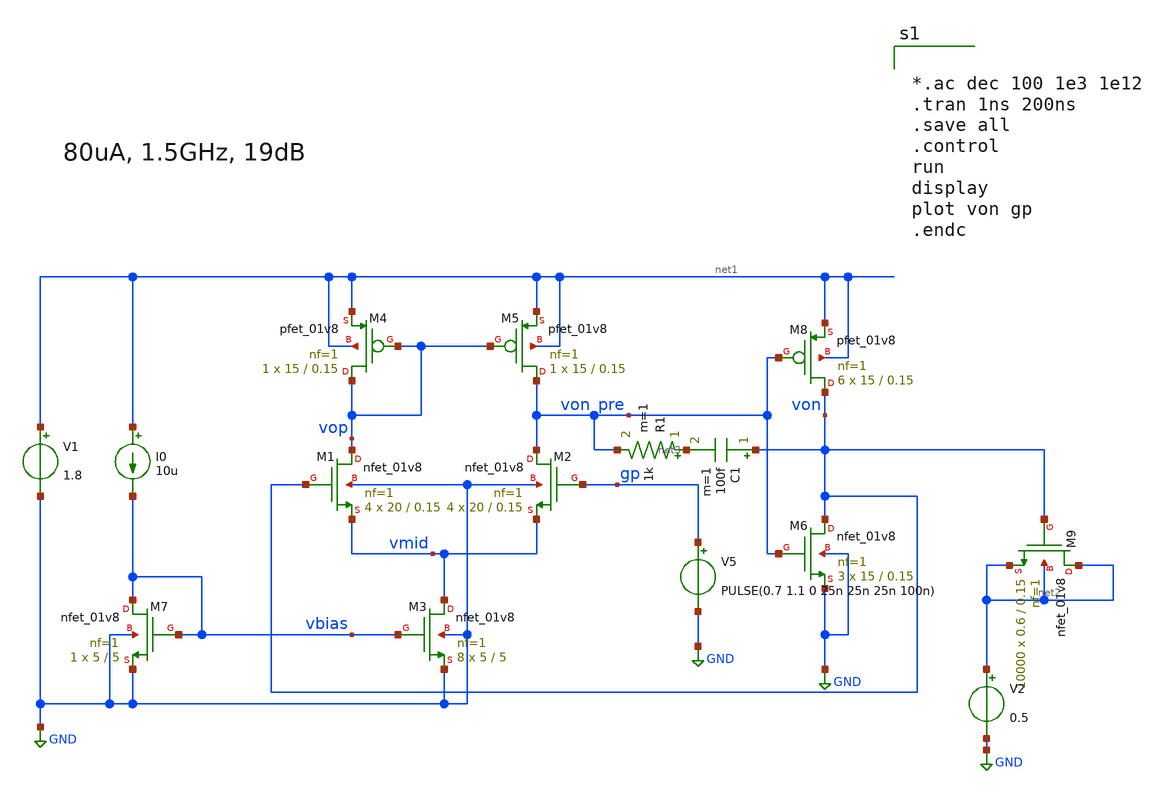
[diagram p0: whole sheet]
** sch_path: xschem/5tamp_fast.sch
**.subckt 5tamp_fast
XM1 vop von vmid GND sky130_fd_pr__nfet_01v8 L=0.15 W=20 nf=1 ad='int((nf+1)/2) * W/nf * 0.29' as='int((nf+2)/2) * W/nf * 0.29'
+ pd='2*int((nf+1)/2) * (W/nf + 0.29)' ps='2*int((nf+2)/2) * (W/nf + 0.29)' nrd='0.29 / W' nrs='0.29 / W'
+ sa=0 sb=0 sd=0 mult=4 m=4
XM2 von_pre gp vmid GND sky130_fd_pr__nfet_01v8 L=0.15 W=20 nf=1 ad='int((nf+1)/2) * W/nf * 0.29' as='int((nf+2)/2) * W/nf * 0.29'
+ pd='2*int((nf+1)/2) * (W/nf + 0.29)' ps='2*int((nf+2)/2) * (W/nf + 0.29)' nrd='0.29 / W' nrs='0.29 / W'
+ sa=0 sb=0 sd=0 mult=4 m=4
XM3 vmid vbias GND GND sky130_fd_pr__nfet_01v8 L=5 W=5 nf=1 ad='int((nf+1)/2) * W/nf * 0.29' as='int((nf+2)/2) * W/nf * 0.29'
+ pd='2*int((nf+1)/2) * (W/nf + 0.29)' ps='2*int((nf+2)/2) * (W/nf + 0.29)' nrd='0.29 / W' nrs='0.29 / W'
+ sa=0 sb=0 sd=0 mult=8 m=8
XM4 vop vop net1 net1 sky130_fd_pr__pfet_01v8 L=0.15 W=15 nf=1 ad='int((nf+1)/2) * W/nf * 0.29' as='int((nf+2)/2) * W/nf * 0.29'
+ pd='2*int((nf+1)/2) * (W/nf + 0.29)' ps='2*int((nf+2)/2) * (W/nf + 0.29)' nrd='0.29 / W' nrs='0.29 / W'
+ sa=0 sb=0 sd=0 mult=1 m=1
XM5 von_pre vop net1 net1 sky130_fd_pr__pfet_01v8 L=0.15 W=15 nf=1 ad='int((nf+1)/2) * W/nf * 0.29' as='int((nf+2)/2) * W/nf * 0.29'
+ pd='2*int((nf+1)/2) * (W/nf + 0.29)' ps='2*int((nf+2)/2) * (W/nf + 0.29)' nrd='0.29 / W' nrs='0.29 / W'
+ sa=0 sb=0 sd=0 mult=1 m=1
V1 net1 GND 1.8
I0 net1 vbias 10u
XM7 vbias vbias GND GND sky130_fd_pr__nfet_01v8 L=5 W=5 nf=1 ad='int((nf+1)/2) * W/nf * 0.29' as='int((nf+2)/2) * W/nf * 0.29'
+ pd='2*int((nf+1)/2) * (W/nf + 0.29)' ps='2*int((nf+2)/2) * (W/nf + 0.29)' nrd='0.29 / W' nrs='0.29 / W'
+ sa=0 sb=0 sd=0 mult=1 m=1
XM6 von von_pre GND GND sky130_fd_pr__nfet_01v8 L=0.15 W=15 nf=1 ad='int((nf+1)/2) * W/nf * 0.29' as='int((nf+2)/2) * W/nf * 0.29'
+ pd='2*int((nf+1)/2) * (W/nf + 0.29)' ps='2*int((nf+2)/2) * (W/nf + 0.29)' nrd='0.29 / W' nrs='0.29 / W'
+ sa=0 sb=0 sd=0 mult=3 m=3
XM8 von von_pre net1 net1 sky130_fd_pr__pfet_01v8 L=0.15 W=15 nf=1 ad='int((nf+1)/2) * W/nf * 0.29' as='int((nf+2)/2) * W/nf * 0.29'
+ pd='2*int((nf+1)/2) * (W/nf + 0.29)' ps='2*int((nf+2)/2) * (W/nf + 0.29)' nrd='0.29 / W' nrs='0.29 / W'
+ sa=0 sb=0 sd=0 mult=6 m=6
V5 gp GND PULSE(0.7 1.1 0 25n 25n 25n 100n)
C1 von net3 100f m=1
R1 net3 von_pre 1k m=1
XM9 net2 von net2 net2 sky130_fd_pr__nfet_01v8 L=0.15 W=0.6 nf=1 ad='int((nf+1)/2) * W/nf * 0.29' as='int((nf+2)/2) * W/nf * 0.29'
+ pd='2*int((nf+1)/2) * (W/nf + 0.29)' ps='2*int((nf+2)/2) * (W/nf + 0.29)' nrd='0.29 / W' nrs='0.29 / W'
+ sa=0 sb=0 sd=0 mult=10000 m=10000
V2 net2 GND 0.5
**** begin user architecture code
.lib $::SKYWATER_MODELS/sky130.lib.spice tt
.include $::PDKPATH/libs.ref/sky130_fd_sc_hvl/spice/sky130_fd_sc_hvl.spice


*.ac dec 100 1e3 1e12
.tran 1ns 200ns
.save all
.control
run
display
plot von gp
.endc


**** end user architecture code
**.ends
.GLOBAL GND
.end
